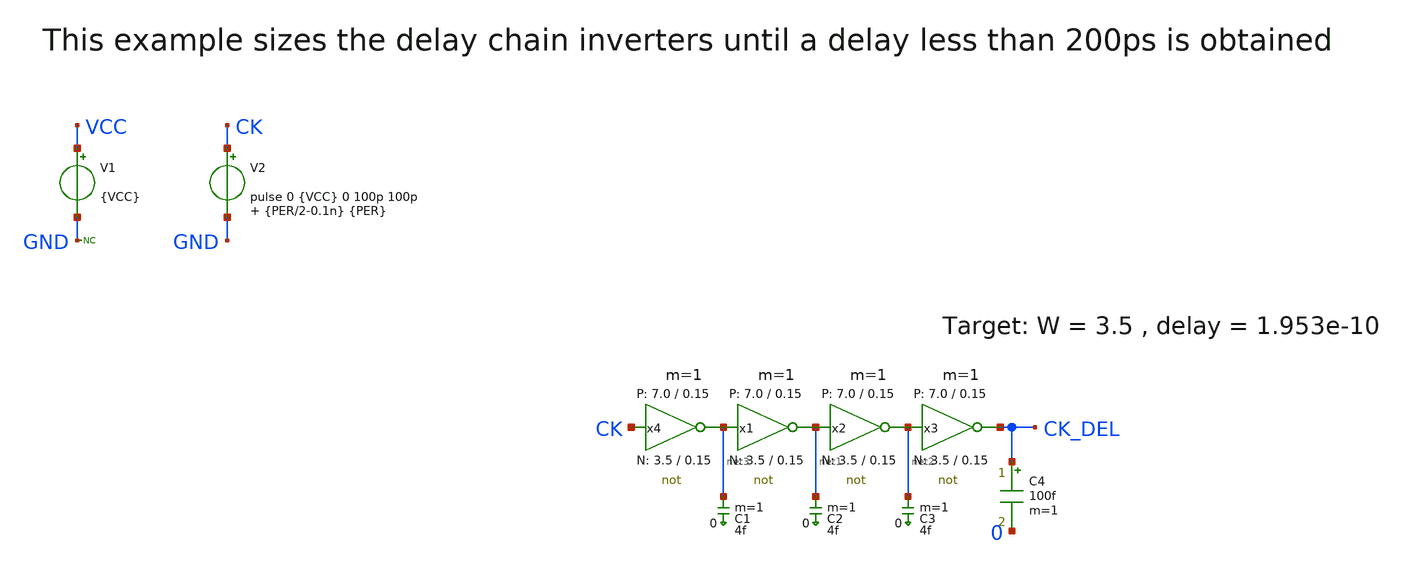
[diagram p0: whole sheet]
** sch_path: sky130A/xschem_libs/sky130_tests_ase/optimize_delay/schematic/optimize_delay.sch
* StefanSchippers/xschem_sky130/sky130_tests/not.sch:
* Copyright 2021 Stefan Frederik Schippers
* Licensed under the Apache License, Version 2.0 (the "License");
**.subckt optimize_delay
V1 VCC GND {VCC}
V2 CK GND pulse 0 {VCC} 0 100p 100p {PER/2-0.1n} {PER}
* noconn GND
C1 net3 0 4f m=1
C2 net1 0 4f m=1
C3 net2 0 4f m=1
x4 net3 CK VCC GND not W_N=3.5 L_N=0.15 W_P=7.0 L_P=0.15 m=1
x1 net1 net3 VCC GND not W_N=3.5 L_N=0.15 W_P=7.0 L_P=0.15 m=1
x2 net2 net1 VCC GND not W_N=3.5 L_N=0.15 W_P=7.0 L_P=0.15 m=1
x3 CK_DEL net2 VCC GND not W_N=3.5 L_N=0.15 W_P=7.0 L_P=0.15 m=1
C4 CK_DEL 0 100f m=1
**.ends

* expanding   symbol:  sky130_tests/not.sym # of pins=2
** sym_path: sky130_tests/not.sym
** sch_path: sky130_tests/not.sch
.subckt not y a VCCPIN VSSPIN     W_N=1 L_N=0.15 W_P=2 L_P=0.15
*.opin y
*.ipin a
XM1 DN a VSSPIN VSSPIN sky130_fd_pr__nfet_01v8 L=L_N W=W_N nf=1 ad='int((1 + 1)/2) * W_N / 1 * 0.29'
+ as='int((1 + 2)/2) * W_N / 1 * 0.29' pd='2*int((1 + 1)/2) * (W_N / 1 + 0.29)' ps='2*int((1 + 2)/2) * (W_N / 1 + 0.29)'
+ nrd='0.29 / W_N ' nrs='0.29 / W_N ' sa=0 sb=0 sd=0 mult=1 m=1
XM2 DP a VCCPIN VCCPIN sky130_fd_pr__pfet_01v8 L=L_P W=W_P nf=1 ad='int((nf+1)/2) * W/nf * 0.29' as='int((nf+2)/2) * W/nf * 0.29'
+ pd='2*int((nf+1)/2) * (W/nf + 0.29)' ps='2*int((nf+2)/2) * (W/nf + 0.29)' nrd='0.29 / W' nrs='0.29 / W'
+ sa=0 sb=0 sd=0 mult=1 m=1
Vmeas DP y 0
.save i(vmeas)
Vmeas1 y DN 0
.save i(vmeas1)
.save v(dp)
.save v(dn)
.ends

.end
